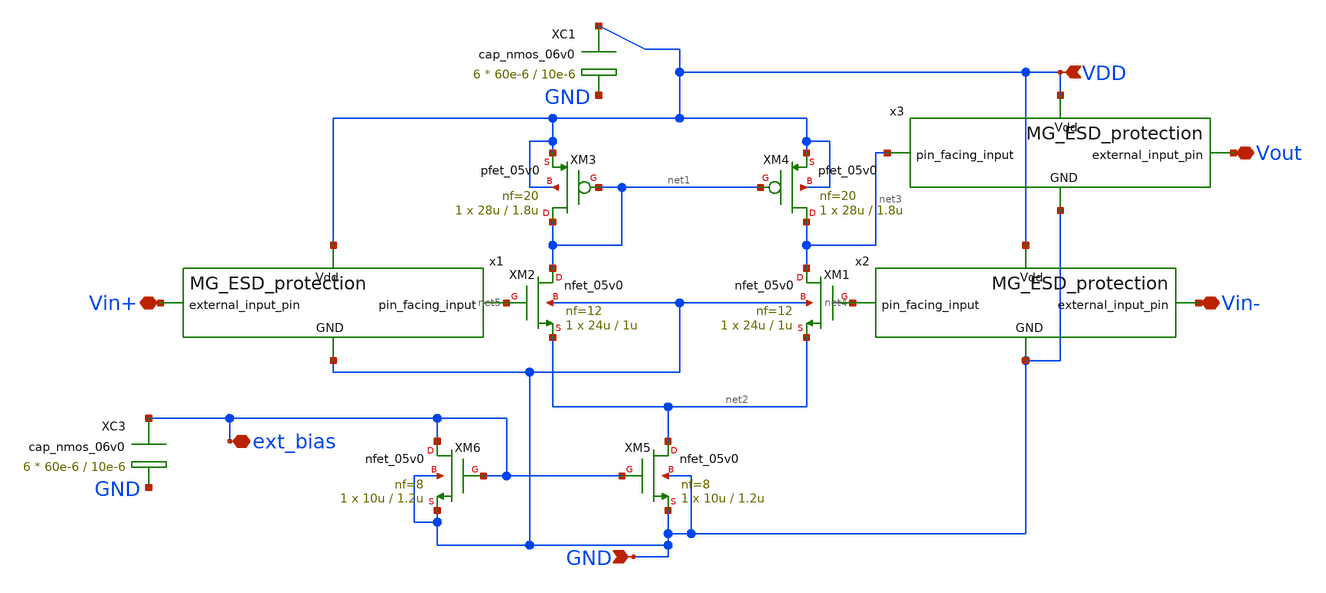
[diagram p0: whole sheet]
** sch_path: TG_gm_ff_testing/gm_ff.sch
**.subckt gm_ff GND VDD ext_bias Vin- Vin+ Vout
*.ipin GND
*.ipin VDD
*.iopin ext_bias
*.iopin Vin-
*.iopin Vin+
*.iopin Vout
XM1 net3 net4 net2 GND nfet_05v0 L=1u W=24u nf=12 ad='int((nf+1)/2) * W/nf * 0.18u' as='int((nf+2)/2) * W/nf * 0.18u'
+ pd='2*int((nf+1)/2) * (W/nf + 0.18u)' ps='2*int((nf+2)/2) * (W/nf + 0.18u)' nrd='0.18u / W' nrs='0.18u / W'
+ sa=0 sb=0 sd=0 m=1
XM2 net1 net5 net2 GND nfet_05v0 L=1u W=24u nf=12 ad='int((nf+1)/2) * W/nf * 0.18u' as='int((nf+2)/2) * W/nf * 0.18u'
+ pd='2*int((nf+1)/2) * (W/nf + 0.18u)' ps='2*int((nf+2)/2) * (W/nf + 0.18u)' nrd='0.18u / W' nrs='0.18u / W'
+ sa=0 sb=0 sd=0 m=1
XM5 net2 ext_bias GND GND nfet_05v0 L=1.2u W=10u nf=8 ad='int((nf+1)/2) * W/nf * 0.18u' as='int((nf+2)/2) * W/nf * 0.18u'
+ pd='2*int((nf+1)/2) * (W/nf + 0.18u)' ps='2*int((nf+2)/2) * (W/nf + 0.18u)' nrd='0.18u / W' nrs='0.18u / W'
+ sa=0 sb=0 sd=0 m=1
XM4 net3 net1 VDD VDD pfet_05v0 L=1.8u W=28u nf=20 ad='int((nf+1)/2) * W/nf * 0.18u' as='int((nf+2)/2) * W/nf * 0.18u'
+ pd='2*int((nf+1)/2) * (W/nf + 0.18u)' ps='2*int((nf+2)/2) * (W/nf + 0.18u)' nrd='0.18u / W' nrs='0.18u / W'
+ sa=0 sb=0 sd=0 m=1
XM3 net1 net1 VDD VDD pfet_05v0 L=1.8u W=28u nf=20 ad='int((nf+1)/2) * W/nf * 0.18u' as='int((nf+2)/2) * W/nf * 0.18u'
+ pd='2*int((nf+1)/2) * (W/nf + 0.18u)' ps='2*int((nf+2)/2) * (W/nf + 0.18u)' nrd='0.18u / W' nrs='0.18u / W'
+ sa=0 sb=0 sd=0 m=1
XM6 ext_bias ext_bias GND GND nfet_05v0 L=1.2u W=10u nf=8 ad='int((nf+1)/2) * W/nf * 0.18u' as='int((nf+2)/2) * W/nf * 0.18u'
+ pd='2*int((nf+1)/2) * (W/nf + 0.18u)' ps='2*int((nf+2)/2) * (W/nf + 0.18u)' nrd='0.18u / W' nrs='0.18u / W'
+ sa=0 sb=0 sd=0 m=1
x1 VDD Vin+ net5 GND MG_ESD_protection
x2 VDD Vin- net4 GND MG_ESD_protection
x3 VDD Vout net3 GND MG_ESD_protection
XC3 ext_bias GND cap_nmos_06v0 c_width=60e-6 c_length=10e-6 m=6
XC1 VDD GND cap_nmos_06v0 c_width=60e-6 c_length=10e-6 m=6
**.ends

* expanding   symbol:
*+  /foss/designs/C05-MRTMOS-SSCS-Chipathon/MG_ESD_protection/MG_ESD_protection.sym # of pins=4
** sym_path: MG_ESD_protection/MG_ESD_protection.sym
** sch_path: MG_ESD_protection/MG_ESD_protection.sch
.subckt MG_ESD_protection Vdd external_input_pin pin_facing_input GND
*.ipin external_input_pin
*.ipin Vdd
*.ipin GND
*.opin pin_facing_input
D2 external_input_pin Vdd diode_nd2ps_06v0 area='1u * 0.6u ' pj='2*1u + 2*0.6u ' m=180
XR2 pin_facing_input external_input_pin GND ppolyf_u_3k r_width=1e-6 r_length=1e-5 m=1
D1 GND external_input_pin diode_nd2ps_06v0 area='1u * 0.6u ' pj='2*1u + 2*0.6u ' m=180
.ends

.end
